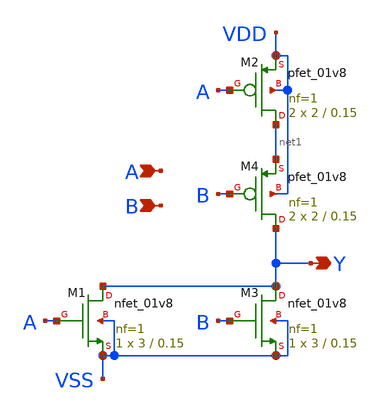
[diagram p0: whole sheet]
** sch_path: layout/xschem/sky130_rhbd/NOR2X1.sch
**.subckt NOR2X1 Y A B
*.opin Y
*.ipin A
*.ipin B
XM1 Y A VSS VSS sky130_fd_pr__nfet_01v8 L=0.15 W=3 nf=1 ad='int((nf+1)/2) * W/nf * 0.29' as='int((nf+2)/2) * W/nf * 0.29'
+ pd='2*int((nf+1)/2) * (W/nf + 0.29)' ps='2*int((nf+2)/2) * (W/nf + 0.29)' nrd='0.29 / W' nrs='0.29 / W'
+ sa=0 sb=0 sd=0 mult=1 m=1
XM2 net1 A VDD VDD sky130_fd_pr__pfet_01v8 L=0.15 W=2 nf=1 ad='int((nf+1)/2) * W/nf * 0.29' as='int((nf+2)/2) * W/nf * 0.29'
+ pd='2*int((nf+1)/2) * (W/nf + 0.29)' ps='2*int((nf+2)/2) * (W/nf + 0.29)' nrd='0.29 / W' nrs='0.29 / W'
+ sa=0 sb=0 sd=0 mult=2 m=2
XM3 Y B VSS VSS sky130_fd_pr__nfet_01v8 L=0.15 W=3 nf=1 ad='int((nf+1)/2) * W/nf * 0.29' as='int((nf+2)/2) * W/nf * 0.29'
+ pd='2*int((nf+1)/2) * (W/nf + 0.29)' ps='2*int((nf+2)/2) * (W/nf + 0.29)' nrd='0.29 / W' nrs='0.29 / W'
+ sa=0 sb=0 sd=0 mult=1 m=1
XM4 Y B net1 VDD sky130_fd_pr__pfet_01v8 L=0.15 W=2 nf=1 ad='int((nf+1)/2) * W/nf * 0.29' as='int((nf+2)/2) * W/nf * 0.29'
+ pd='2*int((nf+1)/2) * (W/nf + 0.29)' ps='2*int((nf+2)/2) * (W/nf + 0.29)' nrd='0.29 / W' nrs='0.29 / W'
+ sa=0 sb=0 sd=0 mult=2 m=2
**.ends
.end
